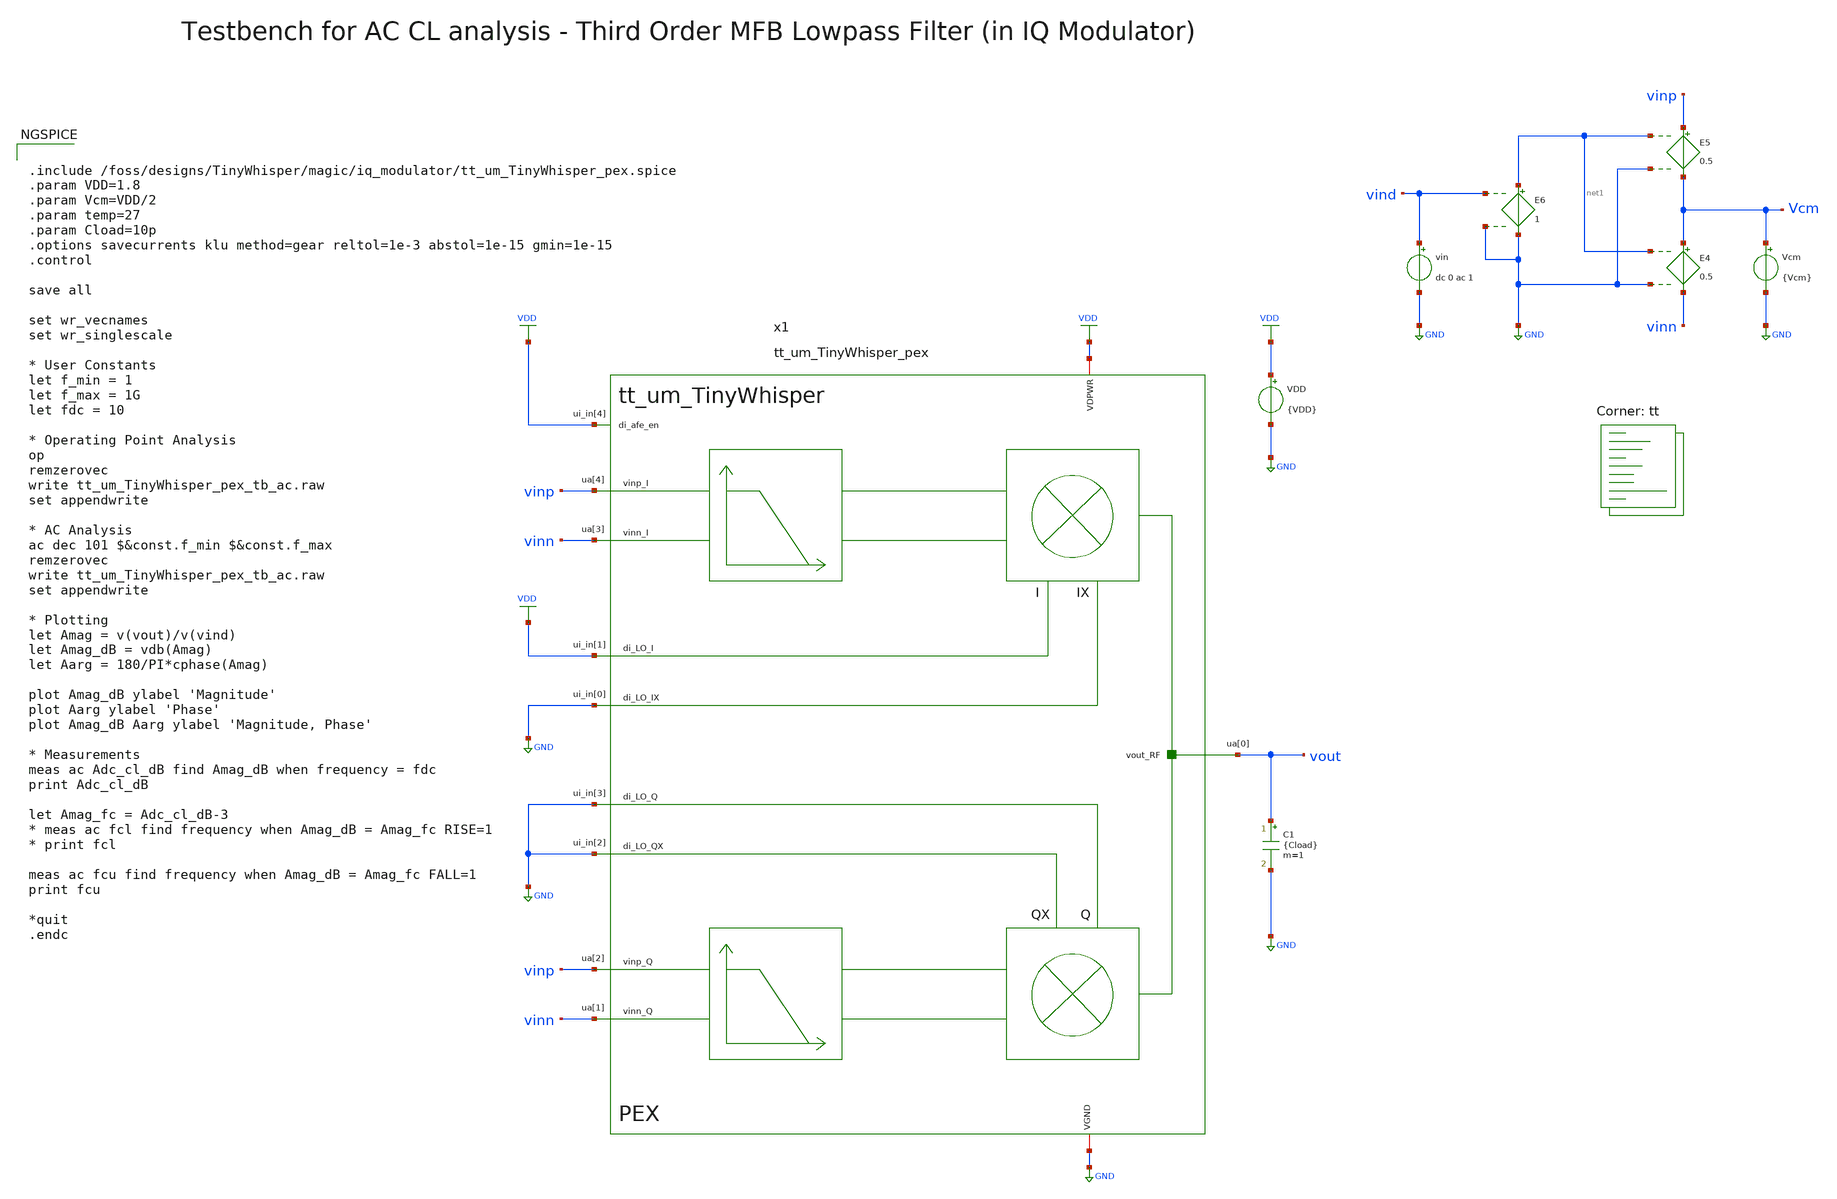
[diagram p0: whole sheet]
** sch_path: magic/iq_modulator/tt_um_TinyWhisper_pex_tb_ac.sch
**.subckt tt_um_TinyWhisper_pex_tb_ac
VDD VDD GND {VDD}
C1 vout GND {Cload} m=1
Vcm Vcm GND {Vcm}
E4 Vcm vinn net1 GND 0.5
E5 vinp Vcm net1 GND 0.5
E6 net1 GND vind GND 1
vin vind GND dc 0 ac 1
x1 VDD VDD vinp vinn VDD GND vout GND GND vinp vinn GND tt_um_TinyWhisper_pex
**** begin user architecture code


.include /foss/designs/TinyWhisper/magic/iq_modulator/tt_um_TinyWhisper_pex.spice
.param VDD=1.8
.param Vcm=VDD/2
.param temp=27
.param Cload=10p
.options savecurrents klu method=gear reltol=1e-3 abstol=1e-15 gmin=1e-15
.control

save all

set wr_vecnames
set wr_singlescale

* User Constants
let f_min = 1
let f_max = 1G
let fdc = 10

* Operating Point Analysis
op
remzerovec
write tt_um_TinyWhisper_pex_tb_ac.raw
set appendwrite

* AC Analysis
ac dec 101 $&const.f_min $&const.f_max
remzerovec
write tt_um_TinyWhisper_pex_tb_ac.raw
set appendwrite

* Plotting
let Amag = v(vout)/v(vind)
let Amag_dB = vdb(Amag)
let Aarg = 180/PI*cphase(Amag)

plot Amag_dB ylabel 'Magnitude'
plot Aarg ylabel 'Phase'
plot Amag_dB Aarg ylabel 'Magnitude, Phase'

* Measurements
meas ac Adc_cl_dB find Amag_dB when frequency = fdc
print Adc_cl_dB

let Amag_fc = Adc_cl_dB-3
* meas ac fcl find frequency when Amag_dB = Amag_fc RISE=1
* print fcl

meas ac fcu find frequency when Amag_dB = Amag_fc FALL=1
print fcu

*quit
.endc


.lib $::SKYWATER_MODELS/sky130.lib.spice tt
**** end user architecture code
**.ends
.GLOBAL GND
.GLOBAL VDD
.end
